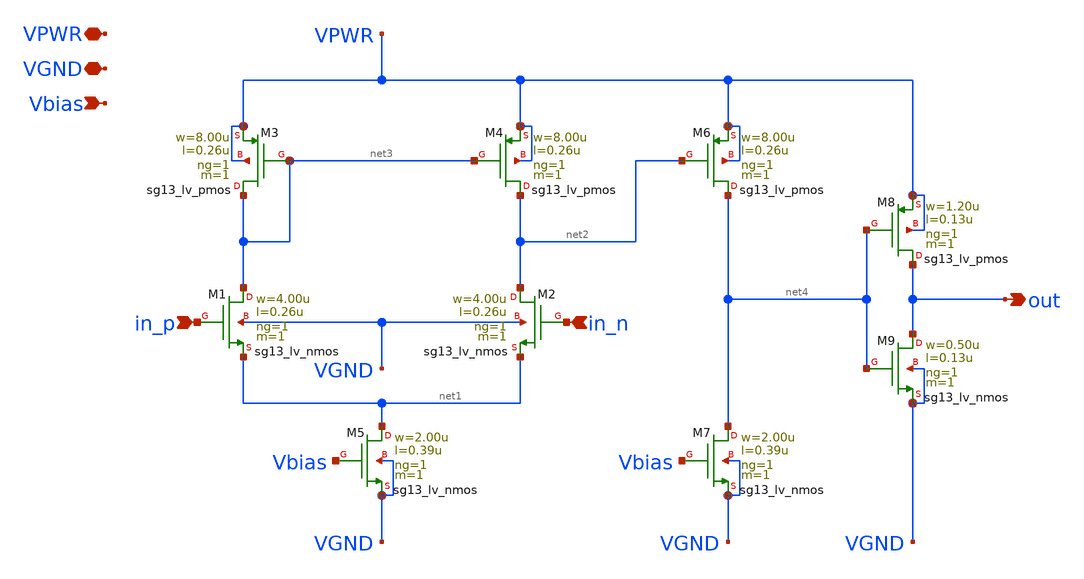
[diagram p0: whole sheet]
** sch_path: xschem/comparator.sch
**.subckt comparator VPWR in_p in_n out VGND Vbias
*.iopin VPWR
*.ipin in_p
*.ipin in_n
*.opin out
*.iopin VGND
*.ipin Vbias
XM1 net3 in_p net1 VGND sg13_lv_nmos w=4.00u l=0.26u ng=1 m=1 mm_ok=1
XM4 net2 net3 VPWR VPWR sg13_lv_pmos w=8.00u l=0.26u ng=1 m=1 mm_ok=1
XM5 net1 Vbias VGND VGND sg13_lv_nmos w=2.00u l=0.39u ng=1 m=1 mm_ok=1
XM2 net2 in_n net1 VGND sg13_lv_nmos w=4.00u l=0.26u ng=1 m=1 mm_ok=1
XM3 net3 net3 VPWR VPWR sg13_lv_pmos w=8.00u l=0.26u ng=1 m=1 mm_ok=1
XM6 net4 net2 VPWR VPWR sg13_lv_pmos w=8.00u l=0.26u ng=1 m=1 mm_ok=1
XM7 net4 Vbias VGND VGND sg13_lv_nmos w=2.00u l=0.39u ng=1 m=1 mm_ok=1
XM8 out net4 VPWR VPWR sg13_lv_pmos w=1.20u l=0.13u ng=1 m=1 mm_ok=1
XM9 out net4 VGND VGND sg13_lv_nmos w=0.50u l=0.13u ng=1 m=1 mm_ok=1
**.ends
.end
